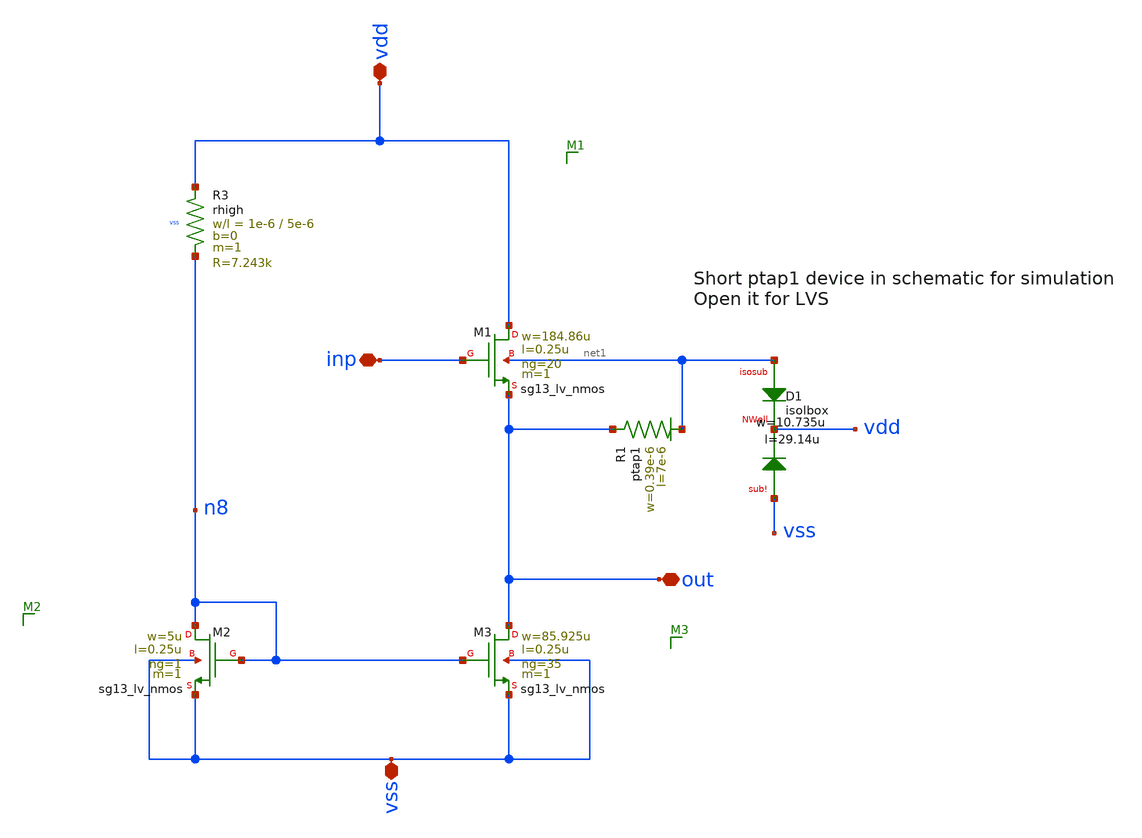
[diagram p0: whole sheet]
** sch_path: LNA7096-main/schematic/xschem/03_sor_foll/sor_foll_out.sch
**.subckt sor_foll_out vdd vss inp out
*.iopin vdd
*.iopin vss
*.iopin inp
*.iopin out
XR3 vdd n8 vss rhigh w=1e-6 l=5e-6 m=1 b=0 mm_ok=1
XM3 out n8 vss vss sg13_lv_nmos w=85.925u l=0.25u ng=35 m=1 mm_ok=1
XM2 n8 n8 vss vss sg13_lv_nmos w=5u l=0.25u ng=1 m=1 mm_ok=1
XM1 vdd inp out net1 sg13_lv_nmos w=184.86u l=0.25u ng=20 m=1 mm_ok=1
XD1 net1 vdd vss isolbox l=29.14u w=10.735u
XR1 out net1 ptap1 R=55.97 w=0.39e-6 l=7e-6
**.ends
.end
